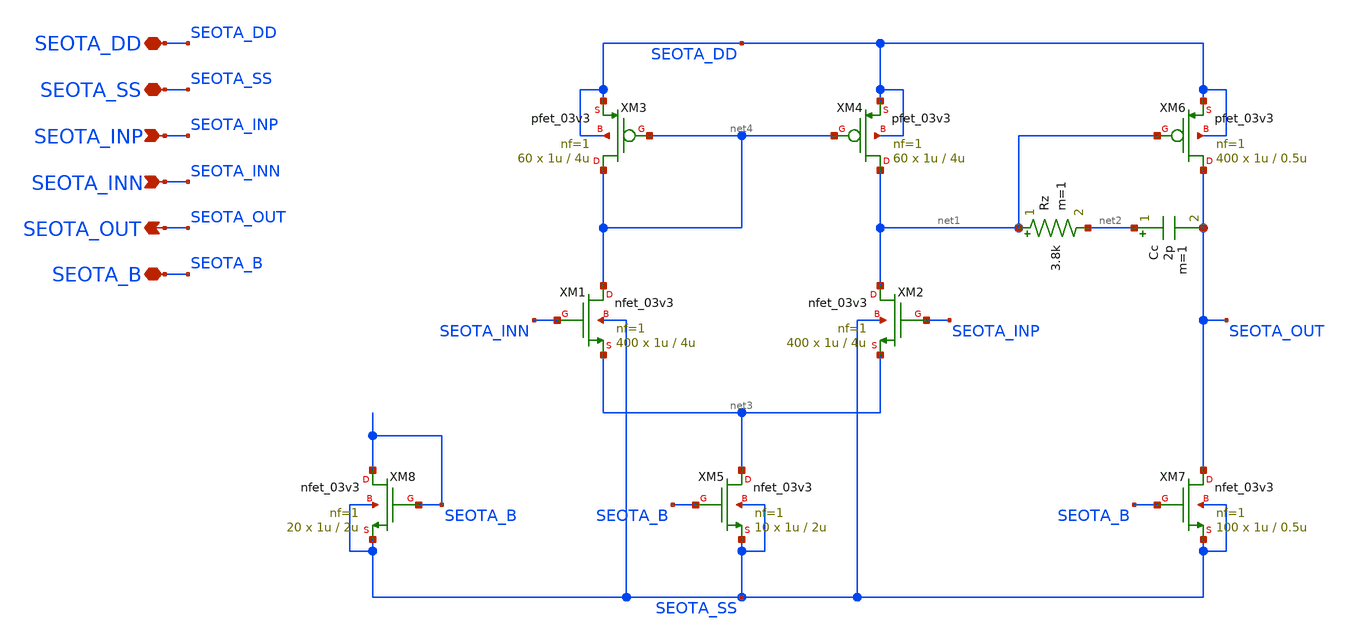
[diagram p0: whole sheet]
** sch_path: Design_Files/IC Design/Schematic/SE_OTA/SE_OTA.sch
**.subckt SE_OTA SEOTA_DD SEOTA_SS SEOTA_INP SEOTA_INN SEOTA_OUT SEOTA_B
*.iopin SEOTA_DD
*.iopin SEOTA_SS
*.ipin SEOTA_INP
*.ipin SEOTA_INN
*.opin SEOTA_OUT
*.iopin SEOTA_B
XM3 net4 net4 SEOTA_DD SEOTA_DD pfet_03v3 L=4u W=1u nf=1 ad='int((nf+1)/2) * W/nf * 0.18u' as='int((nf+2)/2) * W/nf * 0.18u'
+ pd='2*int((nf+1)/2) * (W/nf + 0.18u)' ps='2*int((nf+2)/2) * (W/nf + 0.18u)' nrd='0.18u / W' nrs='0.18u / W'
+ sa=0 sb=0 sd=0 m=60
XM7 SEOTA_OUT SEOTA_B SEOTA_SS SEOTA_SS nfet_03v3 L=0.5u W=1u nf=1 ad='int((nf+1)/2) * W/nf * 0.18u'
+ as='int((nf+2)/2) * W/nf * 0.18u' pd='2*int((nf+1)/2) * (W/nf + 0.18u)' ps='2*int((nf+2)/2) * (W/nf + 0.18u)'
+ nrd='0.18u / W' nrs='0.18u / W' sa=0 sb=0 sd=0 m=100
Rz net1 net2 3.8k m=1
XM5 net3 SEOTA_B SEOTA_SS SEOTA_SS nfet_03v3 L=2u W=1u nf=1 ad='int((nf+1)/2) * W/nf * 0.18u' as='int((nf+2)/2) * W/nf * 0.18u'
+ pd='2*int((nf+1)/2) * (W/nf + 0.18u)' ps='2*int((nf+2)/2) * (W/nf + 0.18u)' nrd='0.18u / W' nrs='0.18u / W'
+ sa=0 sb=0 sd=0 m=10
XM6 SEOTA_OUT net1 SEOTA_DD SEOTA_DD pfet_03v3 L=0.5u W=1u nf=1 ad='int((nf+1)/2) * W/nf * 0.18u' as='int((nf+2)/2) * W/nf * 0.18u'
+ pd='2*int((nf+1)/2) * (W/nf + 0.18u)' ps='2*int((nf+2)/2) * (W/nf + 0.18u)' nrd='0.18u / W' nrs='0.18u / W'
+ sa=0 sb=0 sd=0 m=400
XM8 SEOTA_B SEOTA_B SEOTA_SS SEOTA_SS nfet_03v3 L=2u W=1u nf=1 ad='int((nf+1)/2) * W/nf * 0.18u' as='int((nf+2)/2) * W/nf * 0.18u'
+ pd='2*int((nf+1)/2) * (W/nf + 0.18u)' ps='2*int((nf+2)/2) * (W/nf + 0.18u)' nrd='0.18u / W' nrs='0.18u / W'
+ sa=0 sb=0 sd=0 m=20
Cc net2 SEOTA_OUT 2p m=1
XM4 net1 net4 SEOTA_DD SEOTA_DD pfet_03v3 L=4u W=1u nf=1 ad='int((nf+1)/2) * W/nf * 0.18u' as='int((nf+2)/2) * W/nf * 0.18u'
+ pd='2*int((nf+1)/2) * (W/nf + 0.18u)' ps='2*int((nf+2)/2) * (W/nf + 0.18u)' nrd='0.18u / W' nrs='0.18u / W'
+ sa=0 sb=0 sd=0 m=60
XM1 net4 SEOTA_INN net3 SEOTA_SS nfet_03v3 L=4u W=1u nf=1 ad='int((nf+1)/2) * W/nf * 0.18u' as='int((nf+2)/2) * W/nf * 0.18u'
+ pd='2*int((nf+1)/2) * (W/nf + 0.18u)' ps='2*int((nf+2)/2) * (W/nf + 0.18u)' nrd='0.18u / W' nrs='0.18u / W'
+ sa=0 sb=0 sd=0 m=400
XM2 net1 SEOTA_INP net3 SEOTA_SS nfet_03v3 L=4u W=1u nf=1 ad='int((nf+1)/2) * W/nf * 0.18u' as='int((nf+2)/2) * W/nf * 0.18u'
+ pd='2*int((nf+1)/2) * (W/nf + 0.18u)' ps='2*int((nf+2)/2) * (W/nf + 0.18u)' nrd='0.18u / W' nrs='0.18u / W'
+ sa=0 sb=0 sd=0 m=400
**.ends
.end
